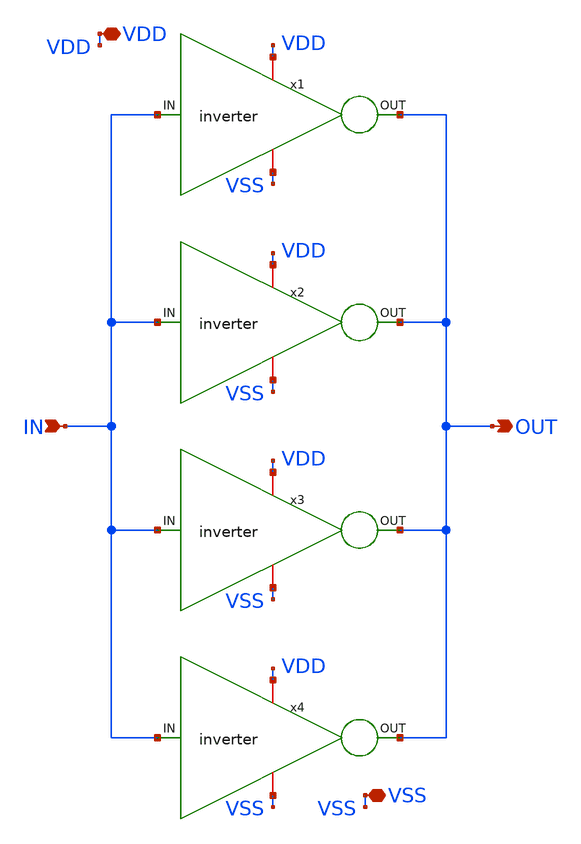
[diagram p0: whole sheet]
** sch_path: design/2x1_mux_with_fo4/fo4_inverter.sch
**.subckt fo4_inverter IN VDD VSS OUT
*.ipin IN
*.iopin VDD
*.iopin VSS
*.opin OUT
x1 VDD OUT IN VSS inverter
x2 VDD OUT IN VSS inverter
x3 VDD OUT IN VSS inverter
x4 VDD OUT IN VSS inverter
**.ends

* expanding   symbol:  inverter.sym # of pins=4
** sym_path: design/ALU/inverter.sym
** sch_path: design/ALU/inverter.sch
.subckt inverter VDD OUT IN VSS
*.ipin IN
*.iopin VDD
*.opin OUT
*.iopin VSS
XM2 OUT IN VDD VDD sky130_fd_pr__pfet_01v8 L=0.15 W=0.9 nf=1 ad='int((nf+1)/2) * W/nf * 0.29' as='int((nf+2)/2) * W/nf * 0.29'
+ pd='2*int((nf+1)/2) * (W/nf + 0.29)' ps='2*int((nf+2)/2) * (W/nf + 0.29)' nrd='0.29 / W' nrs='0.29 / W'
+ sa=0 sb=0 sd=0 mult=1 m=1
XM1 OUT IN VSS VSS sky130_fd_pr__nfet_01v8 L=0.15 W=0.42 nf=1 ad='int((1 + 1)/2) * 0.42 / 1 * 0.29' as='int((1 + 2)/2) * 0.42 / 1 * 0.29'
+ pd='2*int((1 + 1)/2) * (0.42 / 1 + 0.29)' ps='2*int((1 + 2)/2) * (0.42 / 1 + 0.29)' nrd='0.29 / 0.42 '
+ nrs='0.29 / 0.42 ' sa=0 sb=0 sd=0 mult=1 m=1
.ends

.end
